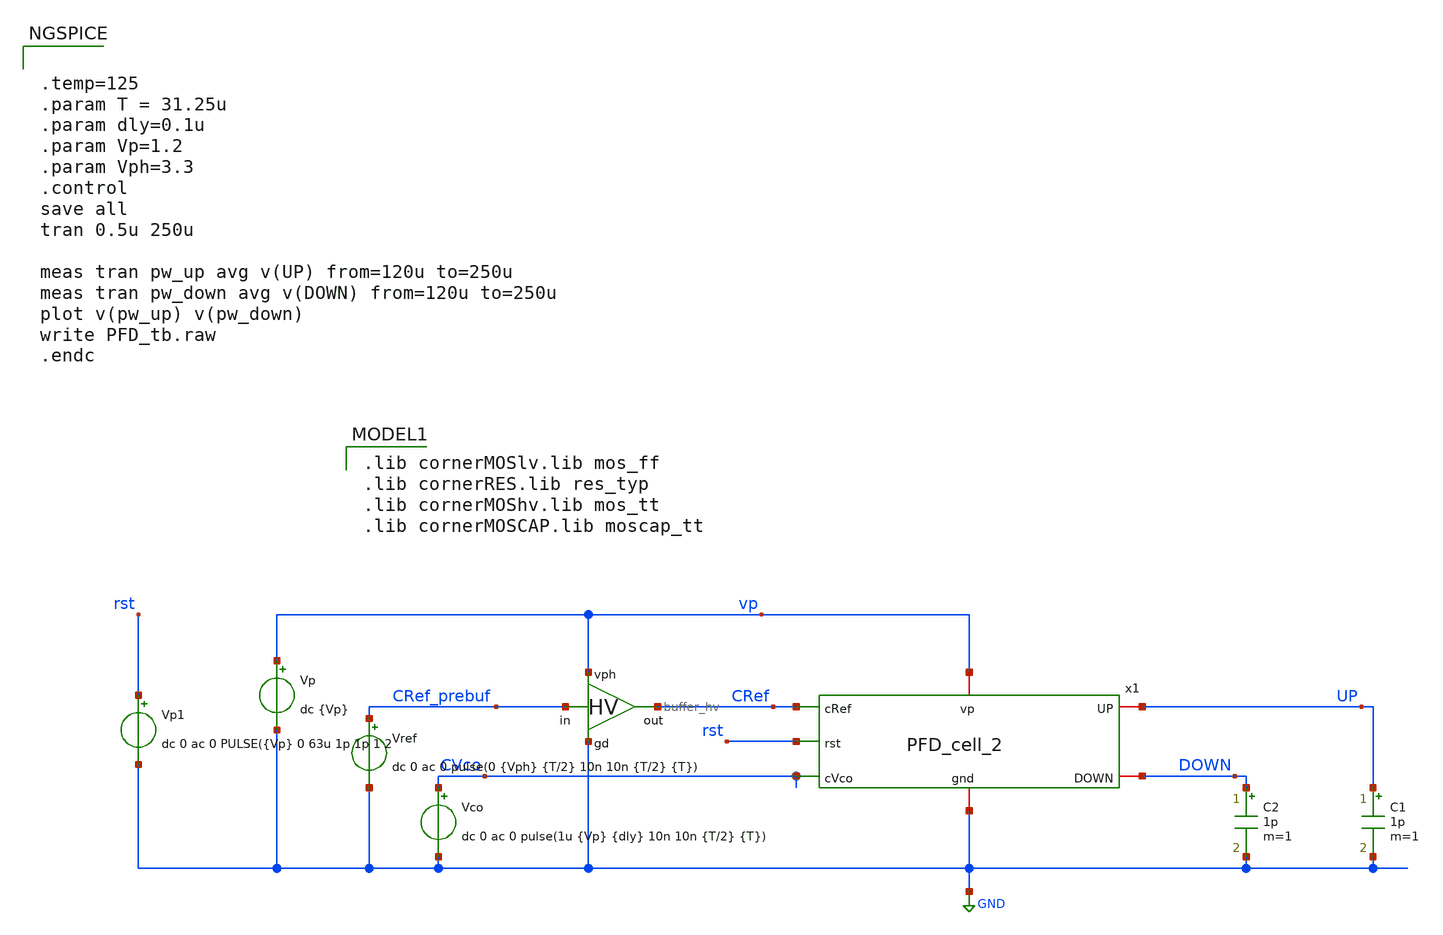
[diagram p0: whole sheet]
** sch_path: PLL0663-main/testbenches/tran/xschem/PFD/PFD_tb.sch
**.subckt PFD_tb
Vref CRef_prebuf GND dc 0 ac 0 pulse(0 {Vph} {T/2} 10n 10n {T/2} {T})
Vco CVco GND dc 0 ac 0 pulse(1u {Vp} {dly} 10n 10n {T/2} {T})
Vp vp GND dc {Vp}
C1 UP GND 1p m=1
C2 DOWN GND 1p m=1
x2 vp CRef_prebuf CRef GND buffer_hv
Vp1 rst GND dc 0 ac 0 PULSE({Vp} 0 63u 1p 1p 1 2
x1 GND vp CRef UP DOWN CVco rst PFD_cell_2
**** begin user architecture code


.temp=125
.param T = 31.25u
.param dly=0.1u
.param Vp=1.2
.param Vph=3.3
.control
save all
tran 0.5u 250u

meas tran pw_up avg v(UP) from=120u to=250u
meas tran pw_down avg v(DOWN) from=120u to=250u
plot v(pw_up) v(pw_down)
write PFD_tb.raw
.endc


 .lib cornerMOSlv.lib mos_ff
.lib cornerRES.lib res_typ
.lib cornerMOShv.lib mos_tt
.lib cornerMOSCAP.lib moscap_tt


**** end user architecture code
**.ends
.GLOBAL GND
.end
